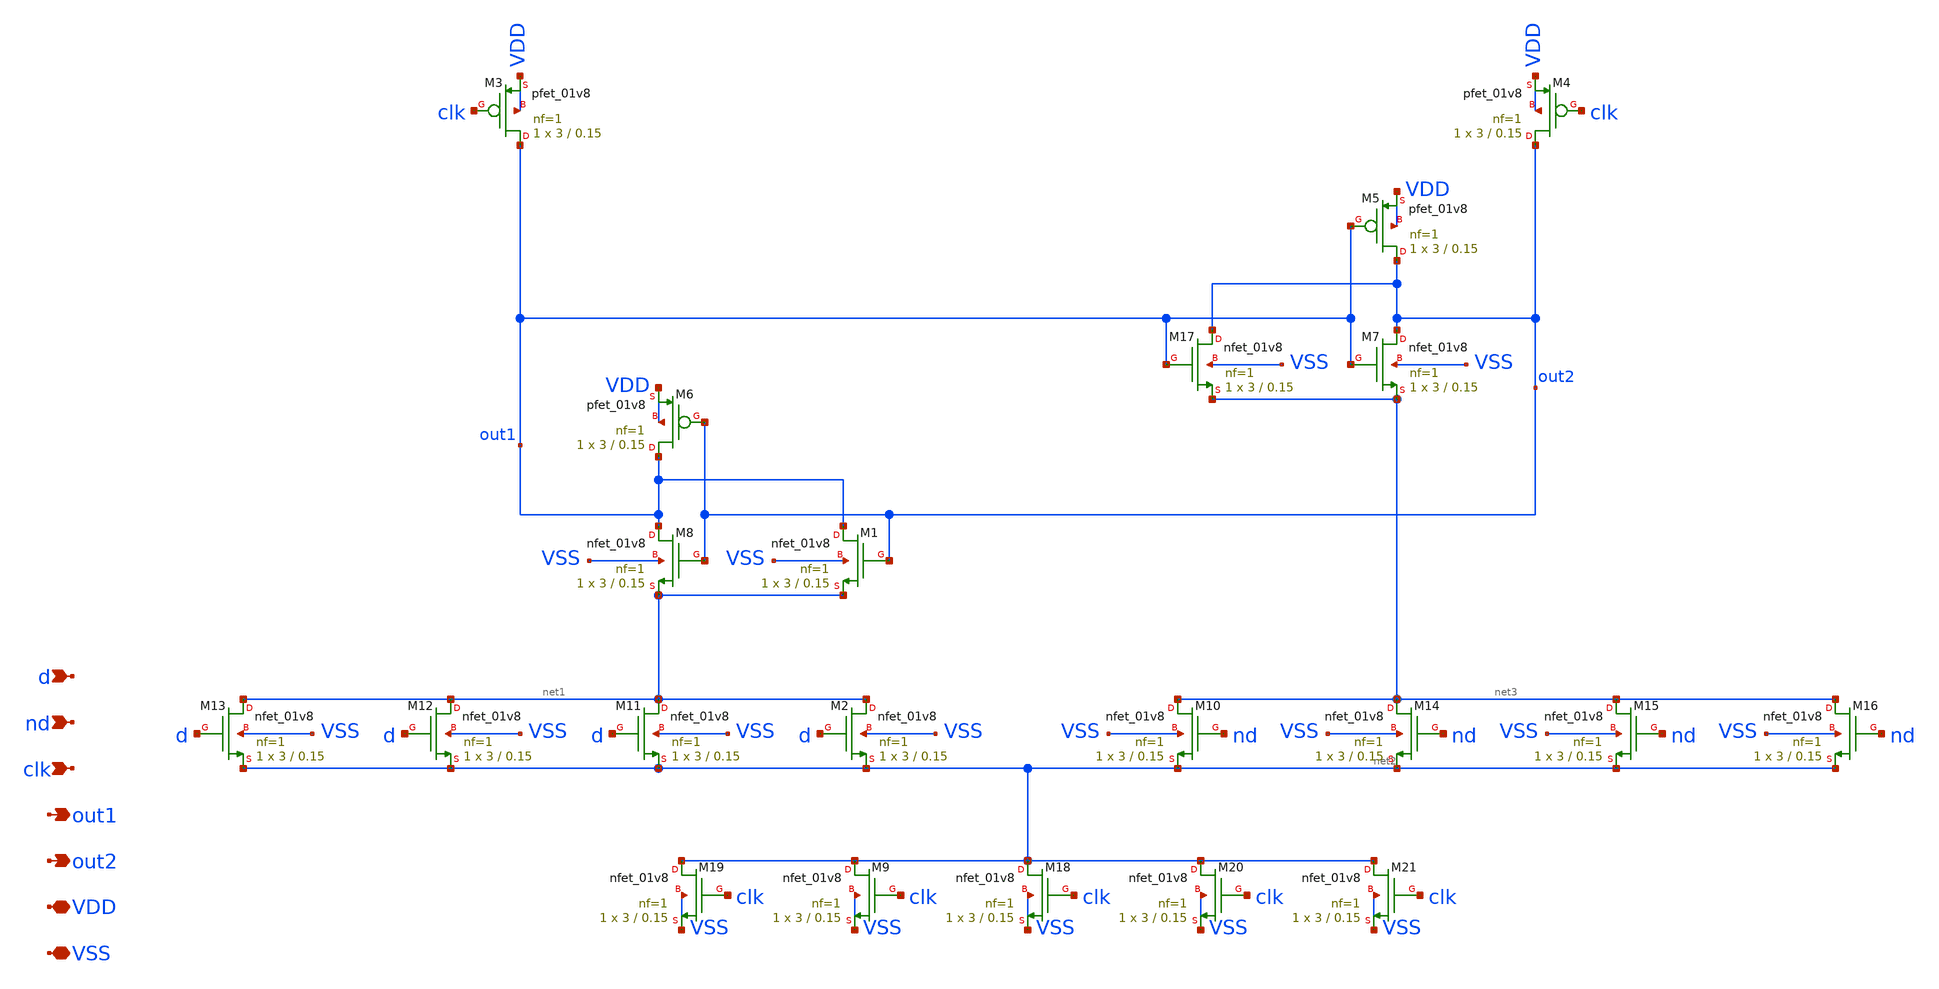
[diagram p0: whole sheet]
** sch_path: xschem/sense_amplifier.sch
**.subckt sense_amplifier VDD d out1 VSS nd clk out2
*.iopin VDD
*.ipin d
*.opin out1
*.iopin VSS
*.ipin nd
*.ipin clk
*.opin out2
XM3 out1 clk VDD VDD sky130_fd_pr__pfet_01v8 L=0.15 W=3 nf=1 ad='int((nf+1)/2) * W/nf * 0.29' as='int((nf+2)/2) * W/nf * 0.29'
+ pd='2*int((nf+1)/2) * (W/nf + 0.29)' ps='2*int((nf+2)/2) * (W/nf + 0.29)' nrd='0.29 / W' nrs='0.29 / W'
+ sa=0 sb=0 sd=0 mult=1 m=1
XM4 out2 clk VDD VDD sky130_fd_pr__pfet_01v8 L=0.15 W=3 nf=1 ad='int((nf+1)/2) * W/nf * 0.29' as='int((nf+2)/2) * W/nf * 0.29'
+ pd='2*int((nf+1)/2) * (W/nf + 0.29)' ps='2*int((nf+2)/2) * (W/nf + 0.29)' nrd='0.29 / W' nrs='0.29 / W'
+ sa=0 sb=0 sd=0 mult=1 m=1
XM5 out2 out1 VDD VDD sky130_fd_pr__pfet_01v8 L=0.15 W=3 nf=1 ad='int((nf+1)/2) * W/nf * 0.29' as='int((nf+2)/2) * W/nf * 0.29'
+ pd='2*int((nf+1)/2) * (W/nf + 0.29)' ps='2*int((nf+2)/2) * (W/nf + 0.29)' nrd='0.29 / W' nrs='0.29 / W'
+ sa=0 sb=0 sd=0 mult=1 m=1
XM6 out1 out2 VDD VDD sky130_fd_pr__pfet_01v8 L=0.15 W=3 nf=1 ad='int((nf+1)/2) * W/nf * 0.29' as='int((nf+2)/2) * W/nf * 0.29'
+ pd='2*int((nf+1)/2) * (W/nf + 0.29)' ps='2*int((nf+2)/2) * (W/nf + 0.29)' nrd='0.29 / W' nrs='0.29 / W'
+ sa=0 sb=0 sd=0 mult=1 m=1
XM7 out2 out1 net3 VSS sky130_fd_pr__nfet_01v8 L=0.15 W=3 nf=1 ad='int((nf+1)/2) * W/nf * 0.29' as='int((nf+2)/2) * W/nf * 0.29'
+ pd='2*int((nf+1)/2) * (W/nf + 0.29)' ps='2*int((nf+2)/2) * (W/nf + 0.29)' nrd='0.29 / W' nrs='0.29 / W'
+ sa=0 sb=0 sd=0 mult=1 m=1
XM8 out1 out2 net1 VSS sky130_fd_pr__nfet_01v8 L=0.15 W=3 nf=1 ad='int((nf+1)/2) * W/nf * 0.29' as='int((nf+2)/2) * W/nf * 0.29'
+ pd='2*int((nf+1)/2) * (W/nf + 0.29)' ps='2*int((nf+2)/2) * (W/nf + 0.29)' nrd='0.29 / W' nrs='0.29 / W'
+ sa=0 sb=0 sd=0 mult=1 m=1
XM9 net2 clk VSS VSS sky130_fd_pr__nfet_01v8 L=0.15 W=3 nf=1 ad='int((nf+1)/2) * W/nf * 0.29' as='int((nf+2)/2) * W/nf * 0.29'
+ pd='2*int((nf+1)/2) * (W/nf + 0.29)' ps='2*int((nf+2)/2) * (W/nf + 0.29)' nrd='0.29 / W' nrs='0.29 / W'
+ sa=0 sb=0 sd=0 mult=1 m=1
XM10 net3 nd net2 VSS sky130_fd_pr__nfet_01v8 L=0.15 W=3 nf=1 ad='int((nf+1)/2) * W/nf * 0.29' as='int((nf+2)/2) * W/nf * 0.29'
+ pd='2*int((nf+1)/2) * (W/nf + 0.29)' ps='2*int((nf+2)/2) * (W/nf + 0.29)' nrd='0.29 / W' nrs='0.29 / W'
+ sa=0 sb=0 sd=0 mult=1 m=1
XM11 net1 d net2 VSS sky130_fd_pr__nfet_01v8 L=0.15 W=3 nf=1 ad='int((nf+1)/2) * W/nf * 0.29' as='int((nf+2)/2) * W/nf * 0.29'
+ pd='2*int((nf+1)/2) * (W/nf + 0.29)' ps='2*int((nf+2)/2) * (W/nf + 0.29)' nrd='0.29 / W' nrs='0.29 / W'
+ sa=0 sb=0 sd=0 mult=1 m=1
XM1 out1 out2 net1 VSS sky130_fd_pr__nfet_01v8 L=0.15 W=3 nf=1 ad='int((nf+1)/2) * W/nf * 0.29' as='int((nf+2)/2) * W/nf * 0.29'
+ pd='2*int((nf+1)/2) * (W/nf + 0.29)' ps='2*int((nf+2)/2) * (W/nf + 0.29)' nrd='0.29 / W' nrs='0.29 / W'
+ sa=0 sb=0 sd=0 mult=1 m=1
XM2 net1 d net2 VSS sky130_fd_pr__nfet_01v8 L=0.15 W=3 nf=1 ad='int((nf+1)/2) * W/nf * 0.29' as='int((nf+2)/2) * W/nf * 0.29'
+ pd='2*int((nf+1)/2) * (W/nf + 0.29)' ps='2*int((nf+2)/2) * (W/nf + 0.29)' nrd='0.29 / W' nrs='0.29 / W'
+ sa=0 sb=0 sd=0 mult=1 m=1
XM12 net1 d net2 VSS sky130_fd_pr__nfet_01v8 L=0.15 W=3 nf=1 ad='int((nf+1)/2) * W/nf * 0.29' as='int((nf+2)/2) * W/nf * 0.29'
+ pd='2*int((nf+1)/2) * (W/nf + 0.29)' ps='2*int((nf+2)/2) * (W/nf + 0.29)' nrd='0.29 / W' nrs='0.29 / W'
+ sa=0 sb=0 sd=0 mult=1 m=1
XM13 net1 d net2 VSS sky130_fd_pr__nfet_01v8 L=0.15 W=3 nf=1 ad='int((nf+1)/2) * W/nf * 0.29' as='int((nf+2)/2) * W/nf * 0.29'
+ pd='2*int((nf+1)/2) * (W/nf + 0.29)' ps='2*int((nf+2)/2) * (W/nf + 0.29)' nrd='0.29 / W' nrs='0.29 / W'
+ sa=0 sb=0 sd=0 mult=1 m=1
XM14 net3 nd net2 VSS sky130_fd_pr__nfet_01v8 L=0.15 W=3 nf=1 ad='int((nf+1)/2) * W/nf * 0.29' as='int((nf+2)/2) * W/nf * 0.29'
+ pd='2*int((nf+1)/2) * (W/nf + 0.29)' ps='2*int((nf+2)/2) * (W/nf + 0.29)' nrd='0.29 / W' nrs='0.29 / W'
+ sa=0 sb=0 sd=0 mult=1 m=1
XM15 net3 nd net2 VSS sky130_fd_pr__nfet_01v8 L=0.15 W=3 nf=1 ad='int((nf+1)/2) * W/nf * 0.29' as='int((nf+2)/2) * W/nf * 0.29'
+ pd='2*int((nf+1)/2) * (W/nf + 0.29)' ps='2*int((nf+2)/2) * (W/nf + 0.29)' nrd='0.29 / W' nrs='0.29 / W'
+ sa=0 sb=0 sd=0 mult=1 m=1
XM16 net3 nd net2 VSS sky130_fd_pr__nfet_01v8 L=0.15 W=3 nf=1 ad='int((nf+1)/2) * W/nf * 0.29' as='int((nf+2)/2) * W/nf * 0.29'
+ pd='2*int((nf+1)/2) * (W/nf + 0.29)' ps='2*int((nf+2)/2) * (W/nf + 0.29)' nrd='0.29 / W' nrs='0.29 / W'
+ sa=0 sb=0 sd=0 mult=1 m=1
XM17 out2 out1 net3 VSS sky130_fd_pr__nfet_01v8 L=0.15 W=3 nf=1 ad='int((nf+1)/2) * W/nf * 0.29' as='int((nf+2)/2) * W/nf * 0.29'
+ pd='2*int((nf+1)/2) * (W/nf + 0.29)' ps='2*int((nf+2)/2) * (W/nf + 0.29)' nrd='0.29 / W' nrs='0.29 / W'
+ sa=0 sb=0 sd=0 mult=1 m=1
XM18 net2 clk VSS VSS sky130_fd_pr__nfet_01v8 L=0.15 W=3 nf=1 ad='int((nf+1)/2) * W/nf * 0.29' as='int((nf+2)/2) * W/nf * 0.29'
+ pd='2*int((nf+1)/2) * (W/nf + 0.29)' ps='2*int((nf+2)/2) * (W/nf + 0.29)' nrd='0.29 / W' nrs='0.29 / W'
+ sa=0 sb=0 sd=0 mult=1 m=1
XM19 net2 clk VSS VSS sky130_fd_pr__nfet_01v8 L=0.15 W=3 nf=1 ad='int((nf+1)/2) * W/nf * 0.29' as='int((nf+2)/2) * W/nf * 0.29'
+ pd='2*int((nf+1)/2) * (W/nf + 0.29)' ps='2*int((nf+2)/2) * (W/nf + 0.29)' nrd='0.29 / W' nrs='0.29 / W'
+ sa=0 sb=0 sd=0 mult=1 m=1
XM20 net2 clk VSS VSS sky130_fd_pr__nfet_01v8 L=0.15 W=3 nf=1 ad='int((nf+1)/2) * W/nf * 0.29' as='int((nf+2)/2) * W/nf * 0.29'
+ pd='2*int((nf+1)/2) * (W/nf + 0.29)' ps='2*int((nf+2)/2) * (W/nf + 0.29)' nrd='0.29 / W' nrs='0.29 / W'
+ sa=0 sb=0 sd=0 mult=1 m=1
XM21 net2 clk VSS VSS sky130_fd_pr__nfet_01v8 L=0.15 W=3 nf=1 ad='int((nf+1)/2) * W/nf * 0.29' as='int((nf+2)/2) * W/nf * 0.29'
+ pd='2*int((nf+1)/2) * (W/nf + 0.29)' ps='2*int((nf+2)/2) * (W/nf + 0.29)' nrd='0.29 / W' nrs='0.29 / W'
+ sa=0 sb=0 sd=0 mult=1 m=1
**.ends
.end
